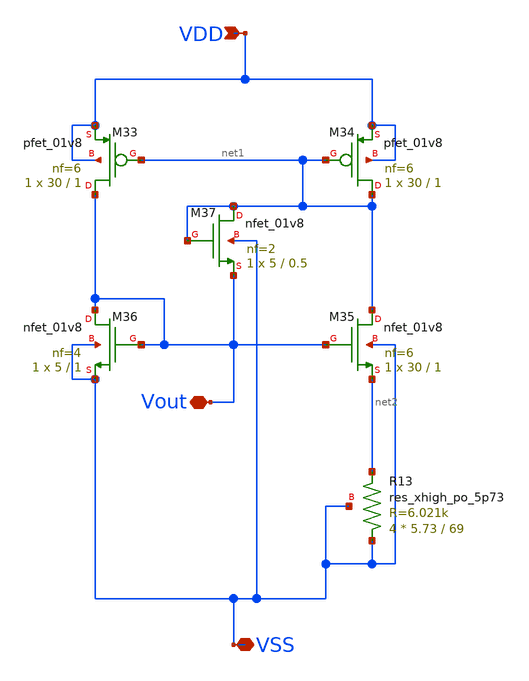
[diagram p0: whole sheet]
** sch_path: SP23_Tapeout/Tapeout_Ready_v5/OTA_GM_Schematic/constant_gm_042123.sch
**.subckt constant_gm_042123 VDD VSS Vout
*.ipin VDD
*.iopin VSS
*.iopin Vout
XM33 Vout net1 VDD VDD sky130_fd_pr__pfet_01v8 L=1 W=30 nf=6 ad='int((nf+1)/2) * W/nf * 0.29' as='int((nf+2)/2) * W/nf * 0.29'
+ pd='2*int((nf+1)/2) * (W/nf + 0.29)' ps='2*int((nf+2)/2) * (W/nf + 0.29)' nrd='0.29 / W' nrs='0.29 / W'
+ sa=0 sb=0 sd=0 mult=1 m=1
XM34 net1 net1 VDD VDD sky130_fd_pr__pfet_01v8 L=1 W=30 nf=6 ad='int((nf+1)/2) * W/nf * 0.29' as='int((nf+2)/2) * W/nf * 0.29'
+ pd='2*int((nf+1)/2) * (W/nf + 0.29)' ps='2*int((nf+2)/2) * (W/nf + 0.29)' nrd='0.29 / W' nrs='0.29 / W'
+ sa=0 sb=0 sd=0 mult=1 m=1
XM35 net1 Vout net2 VSS sky130_fd_pr__nfet_01v8 L=1 W=30 nf=6 ad='int((nf+1)/2) * W/nf * 0.29' as='int((nf+2)/2) * W/nf * 0.29'
+ pd='2*int((nf+1)/2) * (W/nf + 0.29)' ps='2*int((nf+2)/2) * (W/nf + 0.29)' nrd='0.29 / W' nrs='0.29 / W'
+ sa=0 sb=0 sd=0 mult=1 m=1
XM36 Vout Vout VSS VSS sky130_fd_pr__nfet_01v8 L=1 W=5 nf=4 ad='int((nf+1)/2) * W/nf * 0.29' as='int((nf+2)/2) * W/nf * 0.29'
+ pd='2*int((nf+1)/2) * (W/nf + 0.29)' ps='2*int((nf+2)/2) * (W/nf + 0.29)' nrd='0.29 / W' nrs='0.29 / W'
+ sa=0 sb=0 sd=0 mult=1 m=1
XM37 net1 net1 Vout VSS sky130_fd_pr__nfet_01v8 L=0.5 W=5 nf=2 ad='int((nf+1)/2) * W/nf * 0.29' as='int((nf+2)/2) * W/nf * 0.29'
+ pd='2*int((nf+1)/2) * (W/nf + 0.29)' ps='2*int((nf+2)/2) * (W/nf + 0.29)' nrd='0.29 / W' nrs='0.29 / W'
+ sa=0 sb=0 sd=0 mult=1 m=1
XR13 VSS net2 VSS sky130_fd_pr__res_xhigh_po_5p73 L=69 mult=4 m=4
**.ends
.end
